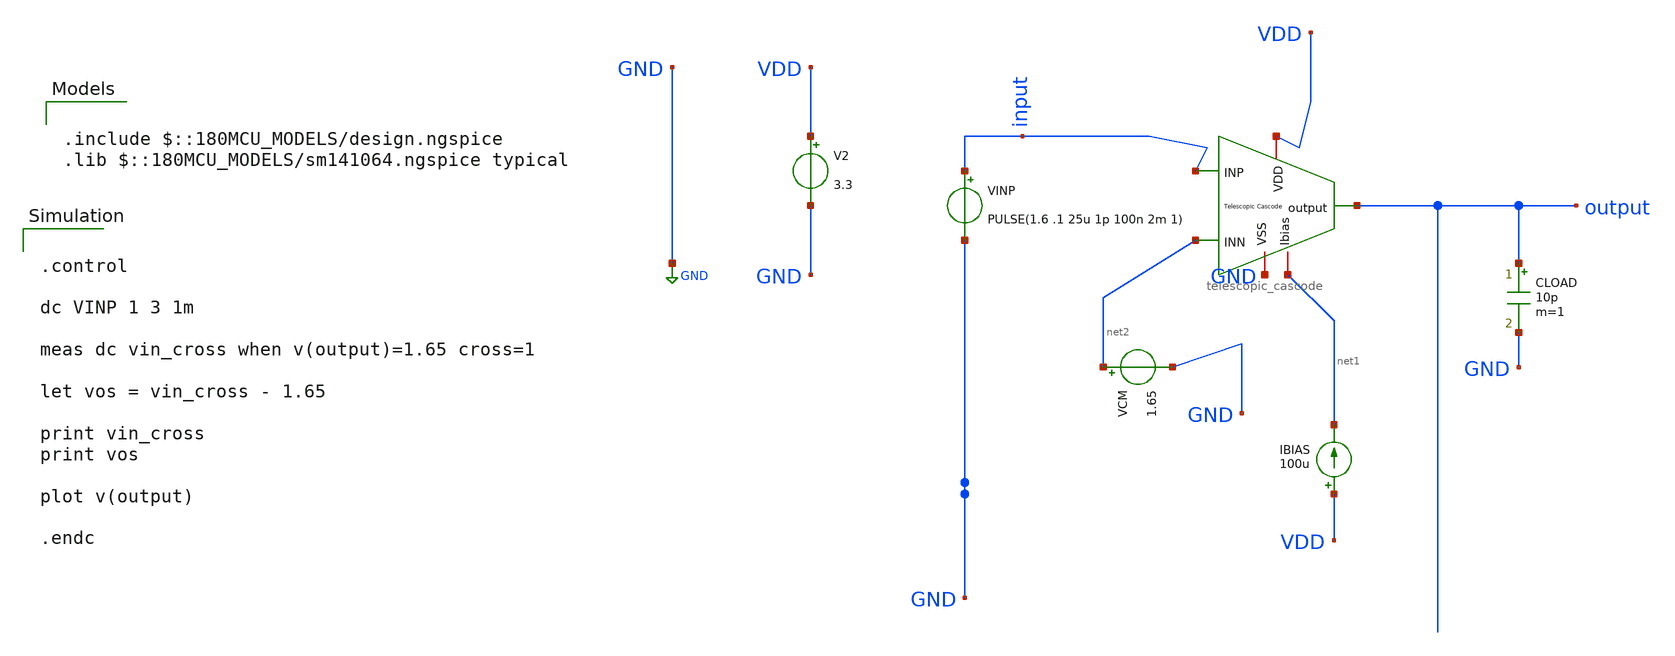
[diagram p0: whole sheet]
** sch_path: designs/libs/core_amps/ota_telescopic/tb/telescopic_vos_tb.sch
**.subckt telescopic_vos_tb
IBIAS VDD net1 100u
V2 VDD GND 3.3
CLOAD output GND 10p m=1
VINP input GND PULSE(1.6 .1 25u 1p 100n 2m 1)
VCM net2 GND 1.65
x1 VDD output net2 input GND net1 telescopic_cascode
**** begin user architecture code

.include $::180MCU_MODELS/design.ngspice
.lib $::180MCU_MODELS/sm141064.ngspice typical



.control

dc VINP 1 3 1m

meas dc vin_cross when v(output)=1.65 cross=1

let vos = vin_cross - 1.65

print vin_cross
print vos

plot v(output)

.endc


**** end user architecture code
**.ends
.GLOBAL GND
.end
